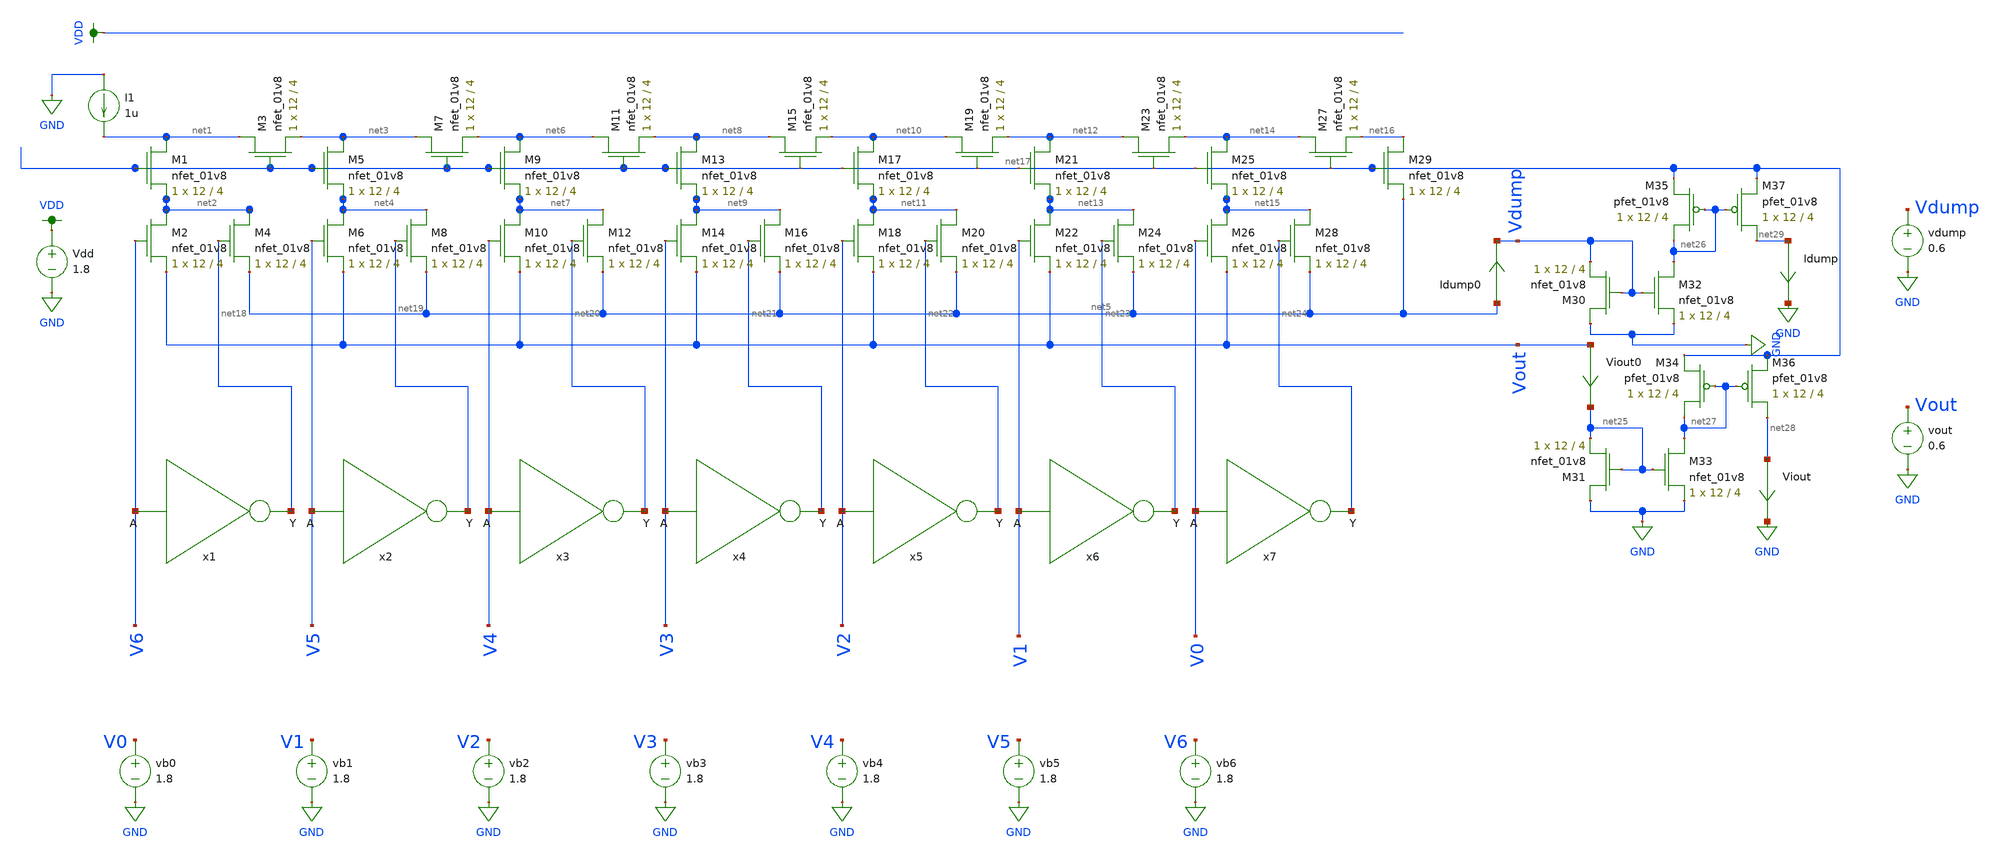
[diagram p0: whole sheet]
** sch_path: xschem/ladder_dac_simulation.sch
**.subckt ladder_dac_simulation
XM1 net1 net17 net2 GND sky130_fd_pr__nfet_01v8 L=4 W=12 nf=1 ad='int((nf+1)/2) * W/nf * 0.29' as='int((nf+2)/2) * W/nf * 0.29'
+ pd='2*int((nf+1)/2) * (W/nf + 0.29)' ps='2*int((nf+2)/2) * (W/nf + 0.29)' nrd='0.29 / W' nrs='0.29 / W'
+ sa=0 sb=0 sd=0 mult=1 m=1
XM3 net1 net17 net3 GND sky130_fd_pr__nfet_01v8 L=4 W=12 nf=1 ad='int((nf+1)/2) * W/nf * 0.29' as='int((nf+2)/2) * W/nf * 0.29'
+ pd='2*int((nf+1)/2) * (W/nf + 0.29)' ps='2*int((nf+2)/2) * (W/nf + 0.29)' nrd='0.29 / W' nrs='0.29 / W'
+ sa=0 sb=0 sd=0 mult=1 m=1
XM5 net3 net17 net4 GND sky130_fd_pr__nfet_01v8 L=4 W=12 nf=1 ad='int((nf+1)/2) * W/nf * 0.29' as='int((nf+2)/2) * W/nf * 0.29'
+ pd='2*int((nf+1)/2) * (W/nf + 0.29)' ps='2*int((nf+2)/2) * (W/nf + 0.29)' nrd='0.29 / W' nrs='0.29 / W'
+ sa=0 sb=0 sd=0 mult=1 m=1
XM7 net3 net17 net6 GND sky130_fd_pr__nfet_01v8 L=4 W=12 nf=1 ad='int((nf+1)/2) * W/nf * 0.29' as='int((nf+2)/2) * W/nf * 0.29'
+ pd='2*int((nf+1)/2) * (W/nf + 0.29)' ps='2*int((nf+2)/2) * (W/nf + 0.29)' nrd='0.29 / W' nrs='0.29 / W'
+ sa=0 sb=0 sd=0 mult=1 m=1
XM6 net4 V5 Vout GND sky130_fd_pr__nfet_01v8 L=4 W=12 nf=1 ad='int((nf+1)/2) * W/nf * 0.29' as='int((nf+2)/2) * W/nf * 0.29'
+ pd='2*int((nf+1)/2) * (W/nf + 0.29)' ps='2*int((nf+2)/2) * (W/nf + 0.29)' nrd='0.29 / W' nrs='0.29 / W'
+ sa=0 sb=0 sd=0 mult=1 m=1
XM8 net4 net19 net5 GND sky130_fd_pr__nfet_01v8 L=4 W=12 nf=1 ad='int((nf+1)/2) * W/nf * 0.29' as='int((nf+2)/2) * W/nf * 0.29'
+ pd='2*int((nf+1)/2) * (W/nf + 0.29)' ps='2*int((nf+2)/2) * (W/nf + 0.29)' nrd='0.29 / W' nrs='0.29 / W'
+ sa=0 sb=0 sd=0 mult=1 m=1
XM2 net2 V6 Vout GND sky130_fd_pr__nfet_01v8 L=4 W=12 nf=1 ad='int((nf+1)/2) * W/nf * 0.29' as='int((nf+2)/2) * W/nf * 0.29'
+ pd='2*int((nf+1)/2) * (W/nf + 0.29)' ps='2*int((nf+2)/2) * (W/nf + 0.29)' nrd='0.29 / W' nrs='0.29 / W'
+ sa=0 sb=0 sd=0 mult=1 m=1
XM4 net2 net18 net5 GND sky130_fd_pr__nfet_01v8 L=4 W=12 nf=1 ad='int((nf+1)/2) * W/nf * 0.29' as='int((nf+2)/2) * W/nf * 0.29'
+ pd='2*int((nf+1)/2) * (W/nf + 0.29)' ps='2*int((nf+2)/2) * (W/nf + 0.29)' nrd='0.29 / W' nrs='0.29 / W'
+ sa=0 sb=0 sd=0 mult=1 m=1
XM9 net6 net17 net7 GND sky130_fd_pr__nfet_01v8 L=4 W=12 nf=1 ad='int((nf+1)/2) * W/nf * 0.29' as='int((nf+2)/2) * W/nf * 0.29'
+ pd='2*int((nf+1)/2) * (W/nf + 0.29)' ps='2*int((nf+2)/2) * (W/nf + 0.29)' nrd='0.29 / W' nrs='0.29 / W'
+ sa=0 sb=0 sd=0 mult=1 m=1
XM11 net6 net17 net8 GND sky130_fd_pr__nfet_01v8 L=4 W=12 nf=1 ad='int((nf+1)/2) * W/nf * 0.29' as='int((nf+2)/2) * W/nf * 0.29'
+ pd='2*int((nf+1)/2) * (W/nf + 0.29)' ps='2*int((nf+2)/2) * (W/nf + 0.29)' nrd='0.29 / W' nrs='0.29 / W'
+ sa=0 sb=0 sd=0 mult=1 m=1
XM10 net7 V4 Vout GND sky130_fd_pr__nfet_01v8 L=4 W=12 nf=1 ad='int((nf+1)/2) * W/nf * 0.29' as='int((nf+2)/2) * W/nf * 0.29'
+ pd='2*int((nf+1)/2) * (W/nf + 0.29)' ps='2*int((nf+2)/2) * (W/nf + 0.29)' nrd='0.29 / W' nrs='0.29 / W'
+ sa=0 sb=0 sd=0 mult=1 m=1
XM12 net7 net20 net5 GND sky130_fd_pr__nfet_01v8 L=4 W=12 nf=1 ad='int((nf+1)/2) * W/nf * 0.29' as='int((nf+2)/2) * W/nf * 0.29'
+ pd='2*int((nf+1)/2) * (W/nf + 0.29)' ps='2*int((nf+2)/2) * (W/nf + 0.29)' nrd='0.29 / W' nrs='0.29 / W'
+ sa=0 sb=0 sd=0 mult=1 m=1
XM13 net8 net17 net9 GND sky130_fd_pr__nfet_01v8 L=4 W=12 nf=1 ad='int((nf+1)/2) * W/nf * 0.29' as='int((nf+2)/2) * W/nf * 0.29'
+ pd='2*int((nf+1)/2) * (W/nf + 0.29)' ps='2*int((nf+2)/2) * (W/nf + 0.29)' nrd='0.29 / W' nrs='0.29 / W'
+ sa=0 sb=0 sd=0 mult=1 m=1
XM15 net8 net17 net10 GND sky130_fd_pr__nfet_01v8 L=4 W=12 nf=1 ad='int((nf+1)/2) * W/nf * 0.29' as='int((nf+2)/2) * W/nf * 0.29'
+ pd='2*int((nf+1)/2) * (W/nf + 0.29)' ps='2*int((nf+2)/2) * (W/nf + 0.29)' nrd='0.29 / W' nrs='0.29 / W'
+ sa=0 sb=0 sd=0 mult=1 m=1
XM14 net9 V3 Vout GND sky130_fd_pr__nfet_01v8 L=4 W=12 nf=1 ad='int((nf+1)/2) * W/nf * 0.29' as='int((nf+2)/2) * W/nf * 0.29'
+ pd='2*int((nf+1)/2) * (W/nf + 0.29)' ps='2*int((nf+2)/2) * (W/nf + 0.29)' nrd='0.29 / W' nrs='0.29 / W'
+ sa=0 sb=0 sd=0 mult=1 m=1
XM16 net9 net21 net5 GND sky130_fd_pr__nfet_01v8 L=4 W=12 nf=1 ad='int((nf+1)/2) * W/nf * 0.29' as='int((nf+2)/2) * W/nf * 0.29'
+ pd='2*int((nf+1)/2) * (W/nf + 0.29)' ps='2*int((nf+2)/2) * (W/nf + 0.29)' nrd='0.29 / W' nrs='0.29 / W'
+ sa=0 sb=0 sd=0 mult=1 m=1
XM17 net10 net17 net11 GND sky130_fd_pr__nfet_01v8 L=4 W=12 nf=1 ad='int((nf+1)/2) * W/nf * 0.29' as='int((nf+2)/2) * W/nf * 0.29'
+ pd='2*int((nf+1)/2) * (W/nf + 0.29)' ps='2*int((nf+2)/2) * (W/nf + 0.29)' nrd='0.29 / W' nrs='0.29 / W'
+ sa=0 sb=0 sd=0 mult=1 m=1
XM19 net10 net17 net12 GND sky130_fd_pr__nfet_01v8 L=4 W=12 nf=1 ad='int((nf+1)/2) * W/nf * 0.29' as='int((nf+2)/2) * W/nf * 0.29'
+ pd='2*int((nf+1)/2) * (W/nf + 0.29)' ps='2*int((nf+2)/2) * (W/nf + 0.29)' nrd='0.29 / W' nrs='0.29 / W'
+ sa=0 sb=0 sd=0 mult=1 m=1
XM18 net11 V2 Vout GND sky130_fd_pr__nfet_01v8 L=4 W=12 nf=1 ad='int((nf+1)/2) * W/nf * 0.29' as='int((nf+2)/2) * W/nf * 0.29'
+ pd='2*int((nf+1)/2) * (W/nf + 0.29)' ps='2*int((nf+2)/2) * (W/nf + 0.29)' nrd='0.29 / W' nrs='0.29 / W'
+ sa=0 sb=0 sd=0 mult=1 m=1
XM20 net11 net22 net5 GND sky130_fd_pr__nfet_01v8 L=4 W=12 nf=1 ad='int((nf+1)/2) * W/nf * 0.29' as='int((nf+2)/2) * W/nf * 0.29'
+ pd='2*int((nf+1)/2) * (W/nf + 0.29)' ps='2*int((nf+2)/2) * (W/nf + 0.29)' nrd='0.29 / W' nrs='0.29 / W'
+ sa=0 sb=0 sd=0 mult=1 m=1
XM21 net12 net17 net13 GND sky130_fd_pr__nfet_01v8 L=4 W=12 nf=1 ad='int((nf+1)/2) * W/nf * 0.29' as='int((nf+2)/2) * W/nf * 0.29'
+ pd='2*int((nf+1)/2) * (W/nf + 0.29)' ps='2*int((nf+2)/2) * (W/nf + 0.29)' nrd='0.29 / W' nrs='0.29 / W'
+ sa=0 sb=0 sd=0 mult=1 m=1
XM23 net12 net17 net14 GND sky130_fd_pr__nfet_01v8 L=4 W=12 nf=1 ad='int((nf+1)/2) * W/nf * 0.29' as='int((nf+2)/2) * W/nf * 0.29'
+ pd='2*int((nf+1)/2) * (W/nf + 0.29)' ps='2*int((nf+2)/2) * (W/nf + 0.29)' nrd='0.29 / W' nrs='0.29 / W'
+ sa=0 sb=0 sd=0 mult=1 m=1
XM22 net13 V1 Vout GND sky130_fd_pr__nfet_01v8 L=4 W=12 nf=1 ad='int((nf+1)/2) * W/nf * 0.29' as='int((nf+2)/2) * W/nf * 0.29'
+ pd='2*int((nf+1)/2) * (W/nf + 0.29)' ps='2*int((nf+2)/2) * (W/nf + 0.29)' nrd='0.29 / W' nrs='0.29 / W'
+ sa=0 sb=0 sd=0 mult=1 m=1
XM24 net13 net23 net5 GND sky130_fd_pr__nfet_01v8 L=4 W=12 nf=1 ad='int((nf+1)/2) * W/nf * 0.29' as='int((nf+2)/2) * W/nf * 0.29'
+ pd='2*int((nf+1)/2) * (W/nf + 0.29)' ps='2*int((nf+2)/2) * (W/nf + 0.29)' nrd='0.29 / W' nrs='0.29 / W'
+ sa=0 sb=0 sd=0 mult=1 m=1
XM25 net14 net17 net15 GND sky130_fd_pr__nfet_01v8 L=4 W=12 nf=1 ad='int((nf+1)/2) * W/nf * 0.29' as='int((nf+2)/2) * W/nf * 0.29'
+ pd='2*int((nf+1)/2) * (W/nf + 0.29)' ps='2*int((nf+2)/2) * (W/nf + 0.29)' nrd='0.29 / W' nrs='0.29 / W'
+ sa=0 sb=0 sd=0 mult=1 m=1
XM27 net14 net17 net16 GND sky130_fd_pr__nfet_01v8 L=4 W=12 nf=1 ad='int((nf+1)/2) * W/nf * 0.29' as='int((nf+2)/2) * W/nf * 0.29'
+ pd='2*int((nf+1)/2) * (W/nf + 0.29)' ps='2*int((nf+2)/2) * (W/nf + 0.29)' nrd='0.29 / W' nrs='0.29 / W'
+ sa=0 sb=0 sd=0 mult=1 m=1
XM26 net15 V0 Vout GND sky130_fd_pr__nfet_01v8 L=4 W=12 nf=1 ad='int((nf+1)/2) * W/nf * 0.29' as='int((nf+2)/2) * W/nf * 0.29'
+ pd='2*int((nf+1)/2) * (W/nf + 0.29)' ps='2*int((nf+2)/2) * (W/nf + 0.29)' nrd='0.29 / W' nrs='0.29 / W'
+ sa=0 sb=0 sd=0 mult=1 m=1
XM28 net15 net24 net5 GND sky130_fd_pr__nfet_01v8 L=4 W=12 nf=1 ad='int((nf+1)/2) * W/nf * 0.29' as='int((nf+2)/2) * W/nf * 0.29'
+ pd='2*int((nf+1)/2) * (W/nf + 0.29)' ps='2*int((nf+2)/2) * (W/nf + 0.29)' nrd='0.29 / W' nrs='0.29 / W'
+ sa=0 sb=0 sd=0 mult=1 m=1
XM29 net16 net17 net5 GND sky130_fd_pr__nfet_01v8 L=4 W=12 nf=1 ad='int((nf+1)/2) * W/nf * 0.29' as='int((nf+2)/2) * W/nf * 0.29'
+ pd='2*int((nf+1)/2) * (W/nf + 0.29)' ps='2*int((nf+2)/2) * (W/nf + 0.29)' nrd='0.29 / W' nrs='0.29 / W'
+ sa=0 sb=0 sd=0 mult=1 m=1
x1 net18 V6 inverter
x2 net19 V5 inverter
x3 net20 V4 inverter
x4 net21 V3 inverter
x5 net22 V2 inverter
x6 net23 V1 inverter
x7 net24 V0 inverter
XM30 GND Vdump Vdump GND sky130_fd_pr__nfet_01v8 L=4 W=12 nf=1 ad='int((nf+1)/2) * W/nf * 0.29' as='int((nf+2)/2) * W/nf * 0.29'
+ pd='2*int((nf+1)/2) * (W/nf + 0.29)' ps='2*int((nf+2)/2) * (W/nf + 0.29)' nrd='0.29 / W' nrs='0.29 / W'
+ sa=0 sb=0 sd=0 mult=1 m=1
XM31 GND net25 net25 GND sky130_fd_pr__nfet_01v8 L=4 W=12 nf=1 ad='int((nf+1)/2) * W/nf * 0.29' as='int((nf+2)/2) * W/nf * 0.29'
+ pd='2*int((nf+1)/2) * (W/nf + 0.29)' ps='2*int((nf+2)/2) * (W/nf + 0.29)' nrd='0.29 / W' nrs='0.29 / W'
+ sa=0 sb=0 sd=0 mult=1 m=1
XM32 net26 Vdump GND GND sky130_fd_pr__nfet_01v8 L=4 W=12 nf=1 ad='int((nf+1)/2) * W/nf * 0.29' as='int((nf+2)/2) * W/nf * 0.29'
+ pd='2*int((nf+1)/2) * (W/nf + 0.29)' ps='2*int((nf+2)/2) * (W/nf + 0.29)' nrd='0.29 / W' nrs='0.29 / W'
+ sa=0 sb=0 sd=0 mult=1 m=1
XM33 net27 net25 GND GND sky130_fd_pr__nfet_01v8 L=4 W=12 nf=1 ad='int((nf+1)/2) * W/nf * 0.29' as='int((nf+2)/2) * W/nf * 0.29'
+ pd='2*int((nf+1)/2) * (W/nf + 0.29)' ps='2*int((nf+2)/2) * (W/nf + 0.29)' nrd='0.29 / W' nrs='0.29 / W'
+ sa=0 sb=0 sd=0 mult=1 m=1
XM35 net26 net26 net17 VDD sky130_fd_pr__pfet_01v8 L=4 W=12 nf=1 ad='int((nf+1)/2) * W/nf * 0.29' as='int((nf+2)/2) * W/nf * 0.29'
+ pd='2*int((nf+1)/2) * (W/nf + 0.29)' ps='2*int((nf+2)/2) * (W/nf + 0.29)' nrd='0.29 / W' nrs='0.29 / W'
+ sa=0 sb=0 sd=0 mult=1 m=1
XM37 net29 net26 net17 VDD sky130_fd_pr__pfet_01v8 L=4 W=12 nf=1 ad='int((nf+1)/2) * W/nf * 0.29' as='int((nf+2)/2) * W/nf * 0.29'
+ pd='2*int((nf+1)/2) * (W/nf + 0.29)' ps='2*int((nf+2)/2) * (W/nf + 0.29)' nrd='0.29 / W' nrs='0.29 / W'
+ sa=0 sb=0 sd=0 mult=1 m=1
XM34 net27 net27 net17 VDD sky130_fd_pr__pfet_01v8 L=4 W=12 nf=1 ad='int((nf+1)/2) * W/nf * 0.29' as='int((nf+2)/2) * W/nf * 0.29'
+ pd='2*int((nf+1)/2) * (W/nf + 0.29)' ps='2*int((nf+2)/2) * (W/nf + 0.29)' nrd='0.29 / W' nrs='0.29 / W'
+ sa=0 sb=0 sd=0 mult=1 m=1
XM36 net28 net27 net17 VDD sky130_fd_pr__pfet_01v8 L=4 W=12 nf=1 ad='int((nf+1)/2) * W/nf * 0.29' as='int((nf+2)/2) * W/nf * 0.29'
+ pd='2*int((nf+1)/2) * (W/nf + 0.29)' ps='2*int((nf+2)/2) * (W/nf + 0.29)' nrd='0.29 / W' nrs='0.29 / W'
+ sa=0 sb=0 sd=0 mult=1 m=1
I1 GND net1 1u
Vdd VDD GND 1.8
vb0 V0 GND 1.8
vb1 V1 GND 1.8
vb2 V2 GND 1.8
vb3 V3 GND 1.8
vb4 V4 GND 1.8
vb5 V5 GND 1.8
vb6 V6 GND 1.8
vdump Vdump GND 0.6
vout Vout GND 0.6
Idump net29 GND 0
.save i(idump)
Viout net28 GND 0
.save i(viout)
Idump0 net5 Vdump 0
.save i(idump0)
Viout0 Vout net25 0
.save i(viout0)
**** begin user architecture code

.option wnflag=1
.param MC_SWITCH=0.0
.lib ~/skywater/skywater-pdk/libraries/sky130_fd_pr_ngspice/latest/models/sky130.lib.spice tt



.control
  set wr_vecnames
  set wr_singlescale
  let code = 0
  while code < 128
    if code eq 0
      let b0 = 0
    else
      let b0 = code % 2
    end
    if floor(code / 2) eq 0
      let b1 = 0
    else
      let b1 = floor(code / 2) % 2
    end
    if floor(code / 4) eq 0
      let b2 = 0
    else
      let b2 = floor(code / 4) % 2
    end
    if floor(code / 8) eq 0
      let b3 = 0
    else
      let b3 = floor(code / 8) % 2
    end
    if floor(code / 16) eq 0
      let b4 = 0
    else
      let b4 = floor(code / 16) % 2
    end
    if floor(code / 32) eq 0
      let b5 = 0
    else
      let b5 = floor(code / 32) % 2
    end
    if floor(code / 64) eq 0
      let b6 = 0
    else
      let b6 = floor(code / 64) % 2
    end
    alter Vb0 1.8*$&b0
    alter Vb1 1.8*$&b1
    alter Vb2 1.8*$&b2
    alter Vb3 1.8*$&b3
    alter Vb4 1.8*$&b4
    alter Vb5 1.8*$&b5
    alter Vb6 1.8*$&b6
    save all
    op
    wrdata ~/Documents/DAC-VLSI/simulation_results/ladder_dac_simulation_andrew.txt v(b0) v(b1)
+ v(b2) v(b3) v(b4) v(b5) v(b6) i(Viout)
    if code eq 0
      set appendwrite
      set wr_vecnames = FALSE
    end
    let code = code + 1
  end
  quit
.endc

**** end user architecture code
**.ends

* expanding   symbol:  ./inverter.sym # of pins=2
** sym_path: xschem/inverter.sym
** sch_path: xschem/inverter.sch
.subckt inverter Y A
*.ipin A
*.opin Y
XM1 Y A VDD VDD sky130_fd_pr__pfet_01v8 L=0.15 W=1 nf=1 ad='int((nf+1)/2) * W/nf * 0.29' as='int((nf+2)/2) * W/nf * 0.29'
+ pd='2*int((nf+1)/2) * (W/nf + 0.29)' ps='2*int((nf+2)/2) * (W/nf + 0.29)' nrd='0.29 / W' nrs='0.29 / W'
+ sa=0 sb=0 sd=0 mult=1 m=1
XM2 Y A GND GND sky130_fd_pr__nfet_01v8 L=0.15 W=1 nf=1 ad='int((nf+1)/2) * W/nf * 0.29' as='int((nf+2)/2) * W/nf * 0.29'
+ pd='2*int((nf+1)/2) * (W/nf + 0.29)' ps='2*int((nf+2)/2) * (W/nf + 0.29)' nrd='0.29 / W' nrs='0.29 / W'
+ sa=0 sb=0 sd=0 mult=1 m=1
.ends

.GLOBAL VDD
.GLOBAL GND
.end
